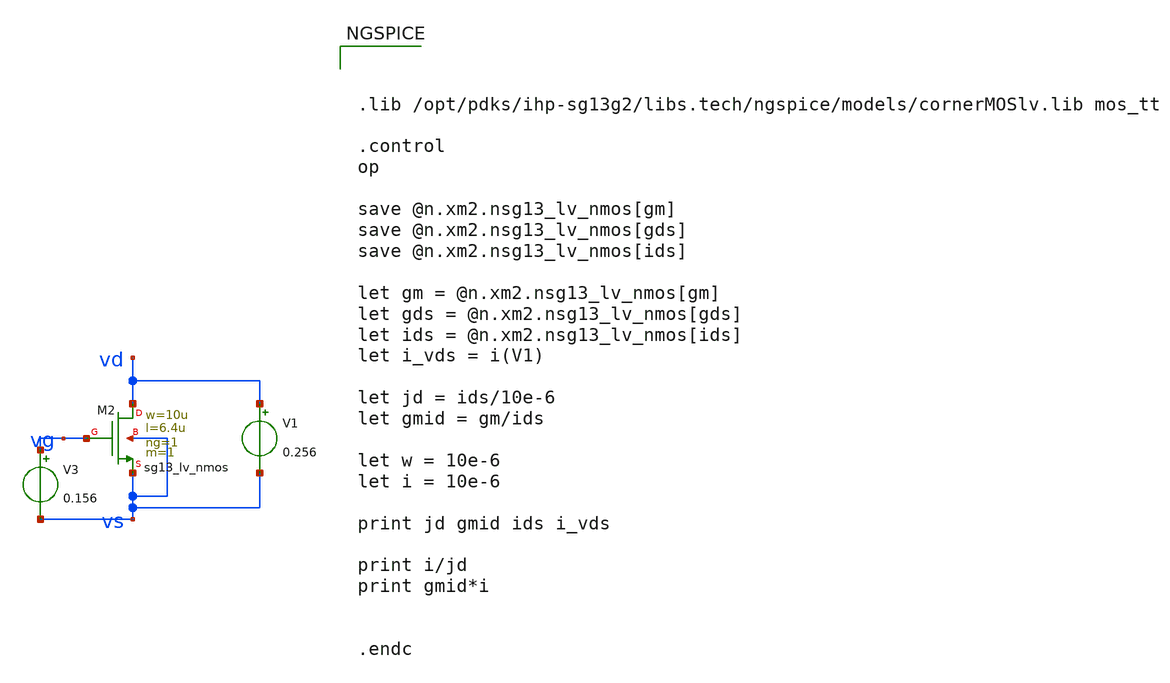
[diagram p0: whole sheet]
** sch_path: test-python/transitor/xschem/nmos_sweep.sch
**.subckt nmos_sweep
XM2 vd vg vs vs sg13_lv_nmos w=10u l=6.4u ng=1 m=1 mm_ok=1
V1 vd vs 0.256
V3 vg vs 0.156
**** begin user architecture code



.lib /opt/pdks/ihp-sg13g2/libs.tech/ngspice/models/cornerMOSlv.lib mos_tt

.control
op

save @n.xm2.nsg13_lv_nmos[gm]
save @n.xm2.nsg13_lv_nmos[gds]
save @n.xm2.nsg13_lv_nmos[ids]

let gm = @n.xm2.nsg13_lv_nmos[gm]
let gds = @n.xm2.nsg13_lv_nmos[gds]
let ids = @n.xm2.nsg13_lv_nmos[ids]
let i_vds = i(V1)

let jd = ids/10e-6
let gmid = gm/ids

let w = 10e-6
let i = 10e-6

print jd gmid ids i_vds

print i/jd
print gmid*i


.endc



**** end user architecture code
**.ends
.end
